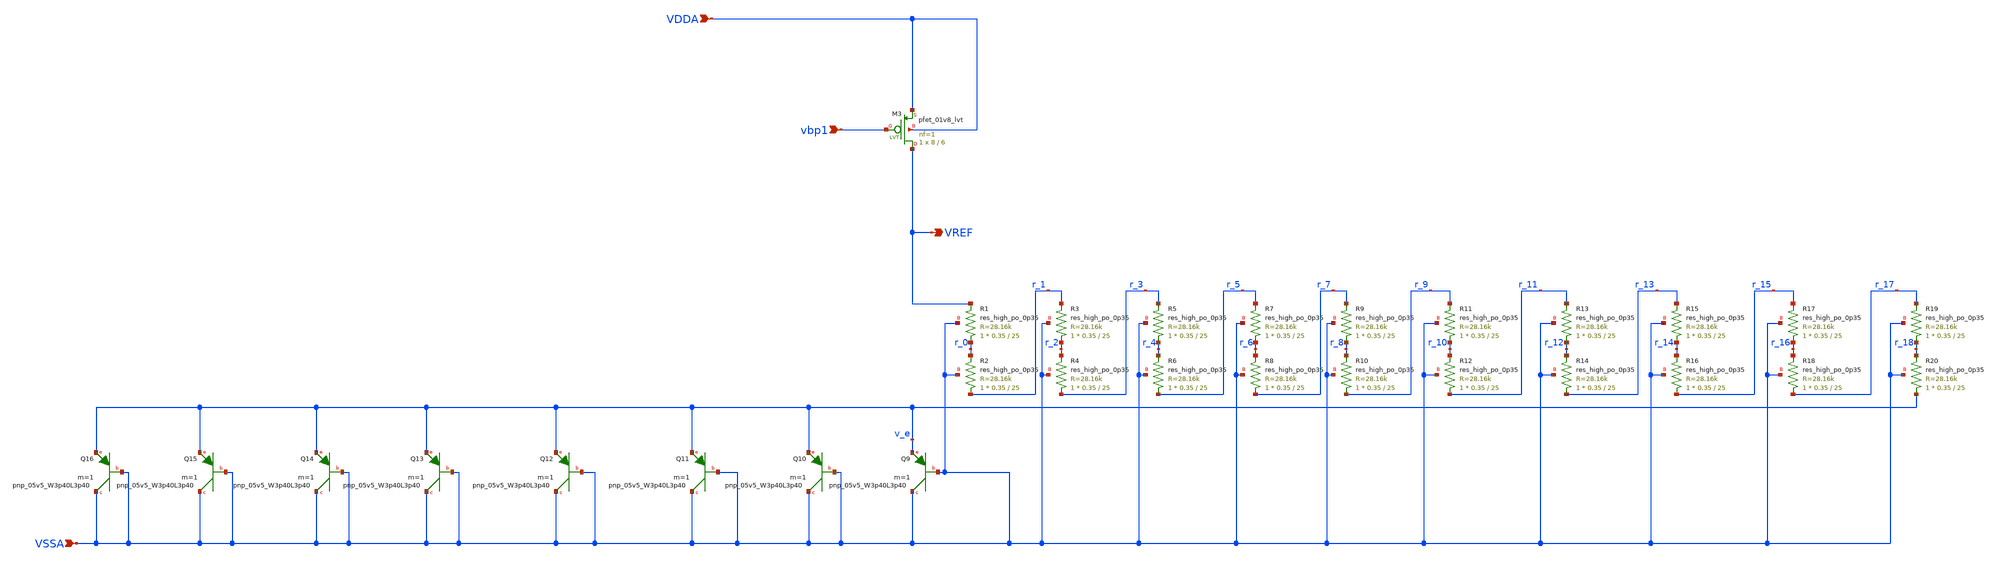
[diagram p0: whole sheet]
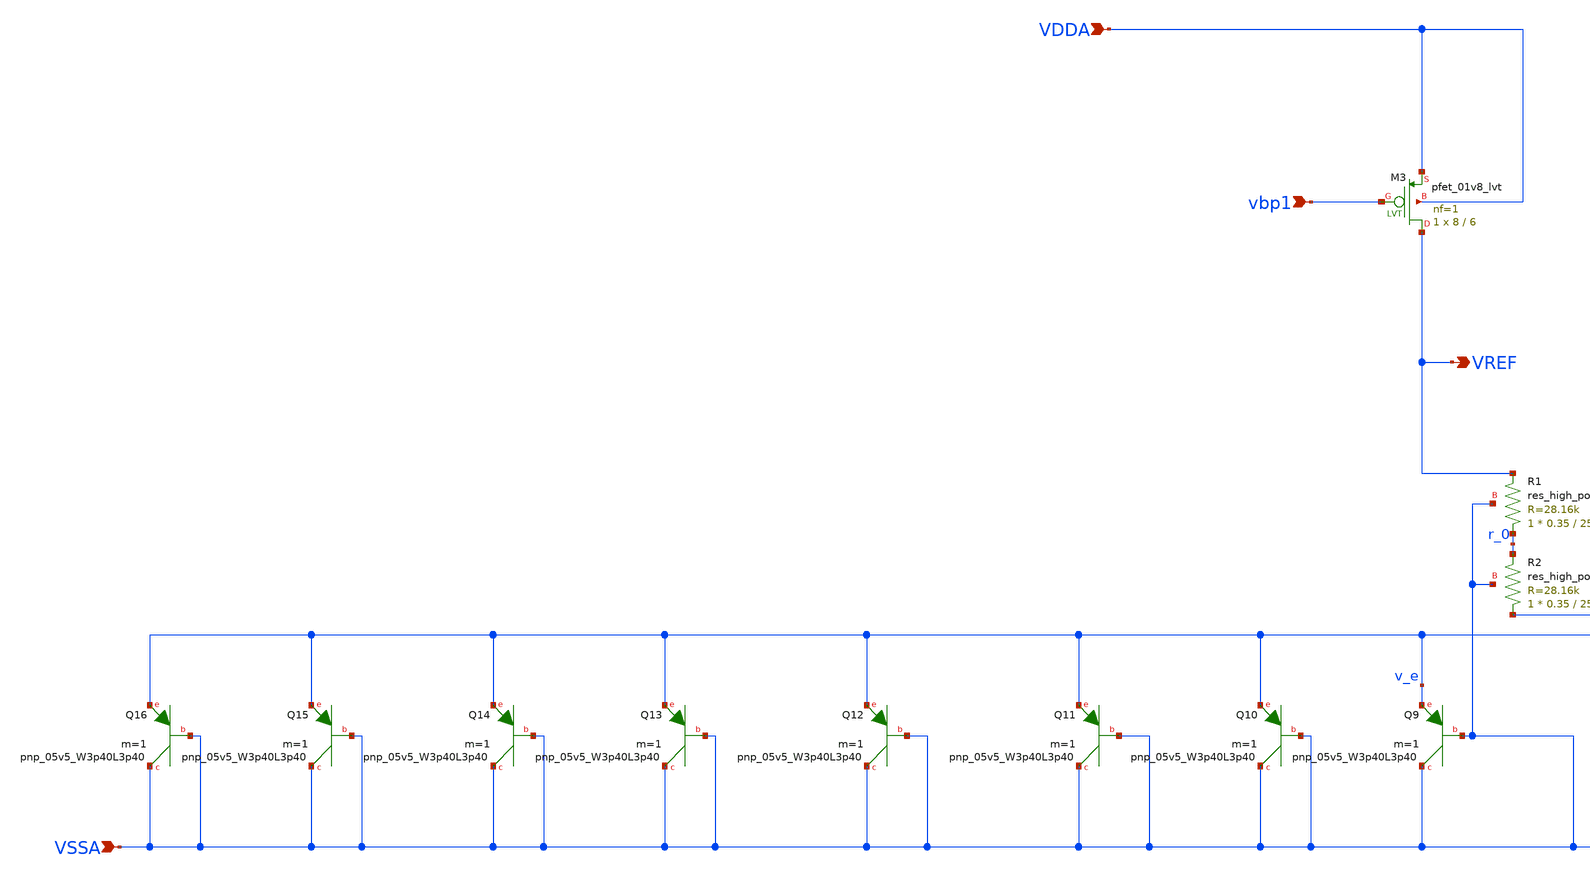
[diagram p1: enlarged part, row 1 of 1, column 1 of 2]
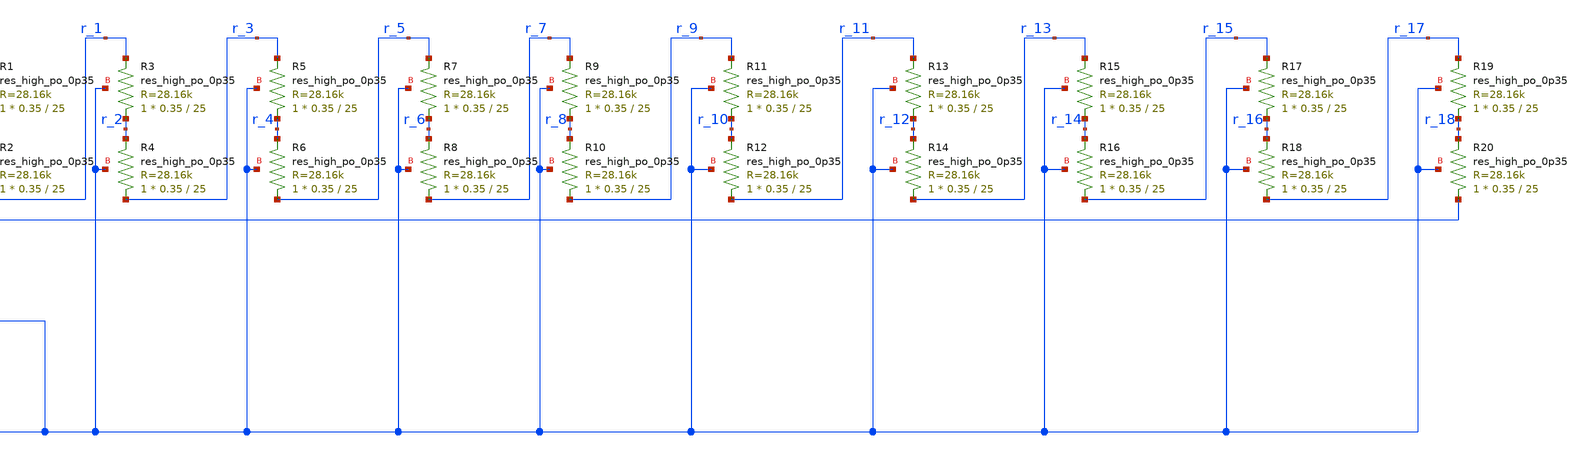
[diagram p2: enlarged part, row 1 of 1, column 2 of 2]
** sch_path: mag/bg_right_branch_lvs.sch
**.subckt bg_right_branch_lvs VSSA VREF VDDA vbp1
*.ipin VSSA
*.opin VREF
*.ipin VDDA
*.ipin vbp1
XQ9 VSSA VSSA v_e sky130_fd_pr__pnp_05v5_W3p40L3p40 m=1
XM3 VREF vbp1 VDDA VDDA sky130_fd_pr__pfet_01v8_lvt L=6 W=8 nf=1 ad='int((1 + 1)/2) * 8 / 1 * 0.29' as='int((1 + 2)/2) * 8 / 1 * 0.29'
+ pd='2*int((1 + 1)/2) * (8 / 1 + 0.29)' ps='2*int((1 + 2)/2) * (8 / 1 + 0.29)' nrd='0.29 / 8 ' nrs='0.29 / 8 '
+ sa=0 sb=0 sd=0 mult=1 m=1
XR1 r_0 VREF VSSA sky130_fd_pr__res_high_po_0p35 L=25 mult=1 m=1
XR2 r_1 r_0 VSSA sky130_fd_pr__res_high_po_0p35 L=25 mult=1 m=1
XR3 r_2 r_1 VSSA sky130_fd_pr__res_high_po_0p35 L=25 mult=1 m=1
XR4 r_3 r_2 VSSA sky130_fd_pr__res_high_po_0p35 L=25 mult=1 m=1
XR5 r_4 r_3 VSSA sky130_fd_pr__res_high_po_0p35 L=25 mult=1 m=1
XR6 r_5 r_4 VSSA sky130_fd_pr__res_high_po_0p35 L=25 mult=1 m=1
XR7 r_6 r_5 VSSA sky130_fd_pr__res_high_po_0p35 L=25 mult=1 m=1
XR8 r_7 r_6 VSSA sky130_fd_pr__res_high_po_0p35 L=25 mult=1 m=1
XR9 r_8 r_7 VSSA sky130_fd_pr__res_high_po_0p35 L=25 mult=1 m=1
XR10 r_9 r_8 VSSA sky130_fd_pr__res_high_po_0p35 L=25 mult=1 m=1
XR11 r_10 r_9 VSSA sky130_fd_pr__res_high_po_0p35 L=25 mult=1 m=1
XR12 r_11 r_10 VSSA sky130_fd_pr__res_high_po_0p35 L=25 mult=1 m=1
XR13 r_12 r_11 VSSA sky130_fd_pr__res_high_po_0p35 L=25 mult=1 m=1
XR14 r_13 r_12 VSSA sky130_fd_pr__res_high_po_0p35 L=25 mult=1 m=1
XR15 r_14 r_13 VSSA sky130_fd_pr__res_high_po_0p35 L=25 mult=1 m=1
XR16 r_15 r_14 VSSA sky130_fd_pr__res_high_po_0p35 L=25 mult=1 m=1
XR17 r_16 r_15 VSSA sky130_fd_pr__res_high_po_0p35 L=25 mult=1 m=1
XR18 r_17 r_16 VSSA sky130_fd_pr__res_high_po_0p35 L=25 mult=1 m=1
XR19 r_18 r_17 VSSA sky130_fd_pr__res_high_po_0p35 L=25 mult=1 m=1
XR20 v_e r_18 VSSA sky130_fd_pr__res_high_po_0p35 L=25 mult=1 m=1
XQ10 VSSA VSSA v_e sky130_fd_pr__pnp_05v5_W3p40L3p40 m=1
XQ11 VSSA VSSA v_e sky130_fd_pr__pnp_05v5_W3p40L3p40 m=1
XQ12 VSSA VSSA v_e sky130_fd_pr__pnp_05v5_W3p40L3p40 m=1
XQ13 VSSA VSSA v_e sky130_fd_pr__pnp_05v5_W3p40L3p40 m=1
XQ14 VSSA VSSA v_e sky130_fd_pr__pnp_05v5_W3p40L3p40 m=1
XQ15 VSSA VSSA v_e sky130_fd_pr__pnp_05v5_W3p40L3p40 m=1
XQ16 VSSA VSSA v_e sky130_fd_pr__pnp_05v5_W3p40L3p40 m=1
**.ends
.end
